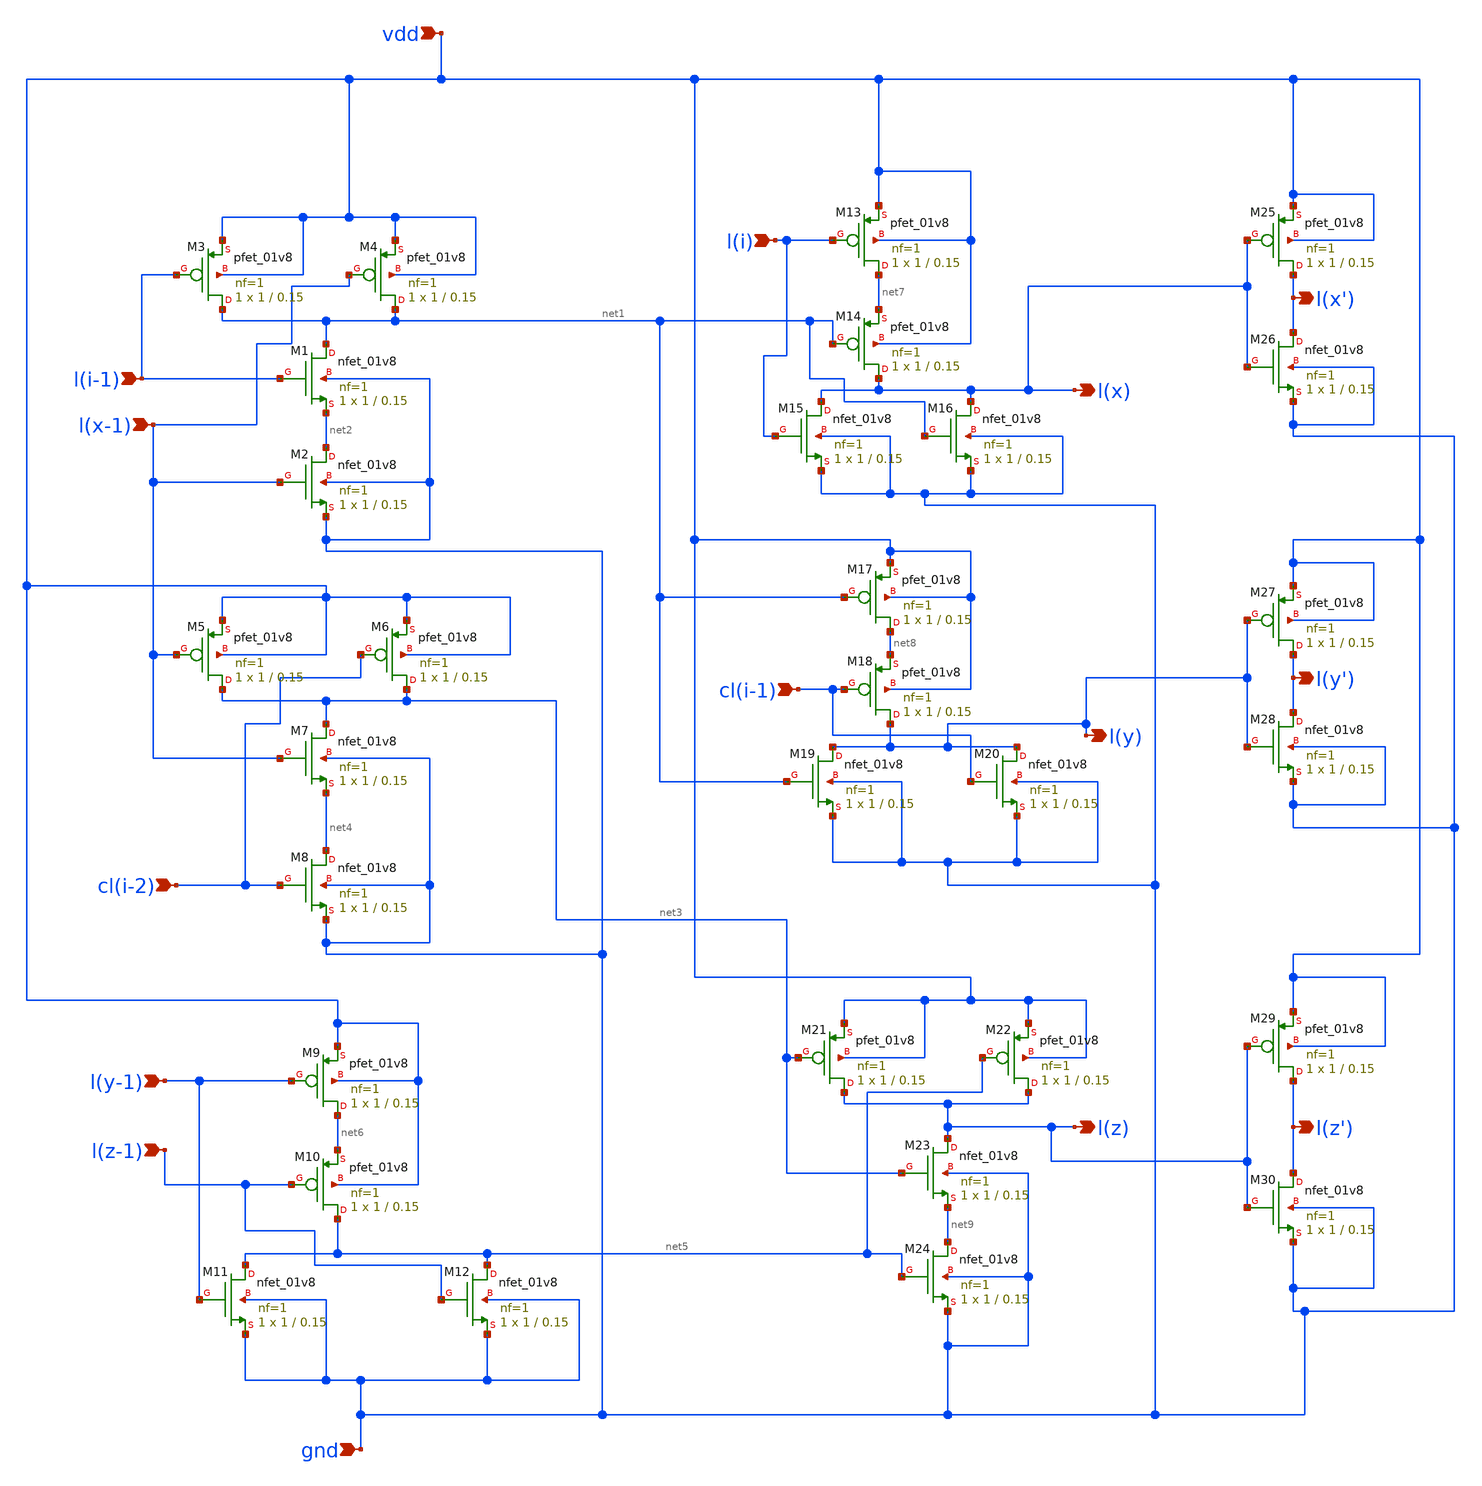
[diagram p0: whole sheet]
** sch_path: config_block2.sch
**.subckt config_block2 l(i-1) l(x-1) l(y-1) l(z-1) vdd gnd l(i) cl(i-1) l(x) l(y) l(z) l(x') l(y') l(z') cl(i-2)
*.ipin l(i-1)
*.ipin l(x-1)
*.ipin l(y-1)
*.ipin l(z-1)
*.ipin vdd
*.ipin gnd
*.ipin l(i)
*.ipin cl(i-1)
*.opin l(x)
*.opin l(y)
*.opin l(z)
*.opin l(x')
*.opin l(y')
*.opin l(z')
*.ipin cl(i-2)
XM1 net1 l(i-1) net2 gnd sky130_fd_pr__nfet_01v8 L=0.15 W=1 nf=1 ad='int((nf+1)/2) * W/nf * 0.29' as='int((nf+2)/2) * W/nf * 0.29'
+ pd='2*int((nf+1)/2) * (W/nf + 0.29)' ps='2*int((nf+2)/2) * (W/nf + 0.29)' nrd='0.29 / W' nrs='0.29 / W'
+ sa=0 sb=0 sd=0 mult=1 m=1
XM2 net2 l(x-1) gnd gnd sky130_fd_pr__nfet_01v8 L=0.15 W=1 nf=1 ad='int((nf+1)/2) * W/nf * 0.29' as='int((nf+2)/2) * W/nf * 0.29'
+ pd='2*int((nf+1)/2) * (W/nf + 0.29)' ps='2*int((nf+2)/2) * (W/nf + 0.29)' nrd='0.29 / W' nrs='0.29 / W'
+ sa=0 sb=0 sd=0 mult=1 m=1
XM3 net1 l(i-1) vdd vdd sky130_fd_pr__pfet_01v8 L=0.15 W=1 nf=1 ad='int((nf+1)/2) * W/nf * 0.29' as='int((nf+2)/2) * W/nf * 0.29'
+ pd='2*int((nf+1)/2) * (W/nf + 0.29)' ps='2*int((nf+2)/2) * (W/nf + 0.29)' nrd='0.29 / W' nrs='0.29 / W'
+ sa=0 sb=0 sd=0 mult=1 m=1
XM4 net1 l(x-1) vdd vdd sky130_fd_pr__pfet_01v8 L=0.15 W=1 nf=1 ad='int((nf+1)/2) * W/nf * 0.29' as='int((nf+2)/2) * W/nf * 0.29'
+ pd='2*int((nf+1)/2) * (W/nf + 0.29)' ps='2*int((nf+2)/2) * (W/nf + 0.29)' nrd='0.29 / W' nrs='0.29 / W'
+ sa=0 sb=0 sd=0 mult=1 m=1
XM5 net3 l(x-1) vdd vdd sky130_fd_pr__pfet_01v8 L=0.15 W=1 nf=1 ad='int((nf+1)/2) * W/nf * 0.29' as='int((nf+2)/2) * W/nf * 0.29'
+ pd='2*int((nf+1)/2) * (W/nf + 0.29)' ps='2*int((nf+2)/2) * (W/nf + 0.29)' nrd='0.29 / W' nrs='0.29 / W'
+ sa=0 sb=0 sd=0 mult=1 m=1
XM6 net3 cl(i-2) vdd vdd sky130_fd_pr__pfet_01v8 L=0.15 W=1 nf=1 ad='int((nf+1)/2) * W/nf * 0.29' as='int((nf+2)/2) * W/nf * 0.29'
+ pd='2*int((nf+1)/2) * (W/nf + 0.29)' ps='2*int((nf+2)/2) * (W/nf + 0.29)' nrd='0.29 / W' nrs='0.29 / W'
+ sa=0 sb=0 sd=0 mult=1 m=1
XM7 net3 l(x-1) net4 gnd sky130_fd_pr__nfet_01v8 L=0.15 W=1 nf=1 ad='int((nf+1)/2) * W/nf * 0.29' as='int((nf+2)/2) * W/nf * 0.29'
+ pd='2*int((nf+1)/2) * (W/nf + 0.29)' ps='2*int((nf+2)/2) * (W/nf + 0.29)' nrd='0.29 / W' nrs='0.29 / W'
+ sa=0 sb=0 sd=0 mult=1 m=1
XM8 net4 cl(i-2) gnd gnd sky130_fd_pr__nfet_01v8 L=0.15 W=1 nf=1 ad='int((nf+1)/2) * W/nf * 0.29' as='int((nf+2)/2) * W/nf * 0.29'
+ pd='2*int((nf+1)/2) * (W/nf + 0.29)' ps='2*int((nf+2)/2) * (W/nf + 0.29)' nrd='0.29 / W' nrs='0.29 / W'
+ sa=0 sb=0 sd=0 mult=1 m=1
XM9 net6 l(y-1) vdd vdd sky130_fd_pr__pfet_01v8 L=0.15 W=1 nf=1 ad='int((nf+1)/2) * W/nf * 0.29' as='int((nf+2)/2) * W/nf * 0.29'
+ pd='2*int((nf+1)/2) * (W/nf + 0.29)' ps='2*int((nf+2)/2) * (W/nf + 0.29)' nrd='0.29 / W' nrs='0.29 / W'
+ sa=0 sb=0 sd=0 mult=1 m=1
XM10 net5 l(z-1) net6 vdd sky130_fd_pr__pfet_01v8 L=0.15 W=1 nf=1 ad='int((nf+1)/2) * W/nf * 0.29' as='int((nf+2)/2) * W/nf * 0.29'
+ pd='2*int((nf+1)/2) * (W/nf + 0.29)' ps='2*int((nf+2)/2) * (W/nf + 0.29)' nrd='0.29 / W' nrs='0.29 / W'
+ sa=0 sb=0 sd=0 mult=1 m=1
XM11 net5 l(y-1) gnd gnd sky130_fd_pr__nfet_01v8 L=0.15 W=1 nf=1 ad='int((nf+1)/2) * W/nf * 0.29' as='int((nf+2)/2) * W/nf * 0.29'
+ pd='2*int((nf+1)/2) * (W/nf + 0.29)' ps='2*int((nf+2)/2) * (W/nf + 0.29)' nrd='0.29 / W' nrs='0.29 / W'
+ sa=0 sb=0 sd=0 mult=1 m=1
XM12 net5 l(z-1) gnd gnd sky130_fd_pr__nfet_01v8 L=0.15 W=1 nf=1 ad='int((nf+1)/2) * W/nf * 0.29' as='int((nf+2)/2) * W/nf * 0.29'
+ pd='2*int((nf+1)/2) * (W/nf + 0.29)' ps='2*int((nf+2)/2) * (W/nf + 0.29)' nrd='0.29 / W' nrs='0.29 / W'
+ sa=0 sb=0 sd=0 mult=1 m=1
XM13 net7 l(i) vdd vdd sky130_fd_pr__pfet_01v8 L=0.15 W=1 nf=1 ad='int((nf+1)/2) * W/nf * 0.29' as='int((nf+2)/2) * W/nf * 0.29'
+ pd='2*int((nf+1)/2) * (W/nf + 0.29)' ps='2*int((nf+2)/2) * (W/nf + 0.29)' nrd='0.29 / W' nrs='0.29 / W'
+ sa=0 sb=0 sd=0 mult=1 m=1
XM14 l(x) net1 net7 vdd sky130_fd_pr__pfet_01v8 L=0.15 W=1 nf=1 ad='int((nf+1)/2) * W/nf * 0.29' as='int((nf+2)/2) * W/nf * 0.29'
+ pd='2*int((nf+1)/2) * (W/nf + 0.29)' ps='2*int((nf+2)/2) * (W/nf + 0.29)' nrd='0.29 / W' nrs='0.29 / W'
+ sa=0 sb=0 sd=0 mult=1 m=1
XM15 l(x) l(i) gnd gnd sky130_fd_pr__nfet_01v8 L=0.15 W=1 nf=1 ad='int((nf+1)/2) * W/nf * 0.29' as='int((nf+2)/2) * W/nf * 0.29'
+ pd='2*int((nf+1)/2) * (W/nf + 0.29)' ps='2*int((nf+2)/2) * (W/nf + 0.29)' nrd='0.29 / W' nrs='0.29 / W'
+ sa=0 sb=0 sd=0 mult=1 m=1
XM16 l(x) net1 gnd gnd sky130_fd_pr__nfet_01v8 L=0.15 W=1 nf=1 ad='int((nf+1)/2) * W/nf * 0.29' as='int((nf+2)/2) * W/nf * 0.29'
+ pd='2*int((nf+1)/2) * (W/nf + 0.29)' ps='2*int((nf+2)/2) * (W/nf + 0.29)' nrd='0.29 / W' nrs='0.29 / W'
+ sa=0 sb=0 sd=0 mult=1 m=1
XM17 net8 net1 vdd vdd sky130_fd_pr__pfet_01v8 L=0.15 W=1 nf=1 ad='int((nf+1)/2) * W/nf * 0.29' as='int((nf+2)/2) * W/nf * 0.29'
+ pd='2*int((nf+1)/2) * (W/nf + 0.29)' ps='2*int((nf+2)/2) * (W/nf + 0.29)' nrd='0.29 / W' nrs='0.29 / W'
+ sa=0 sb=0 sd=0 mult=1 m=1
XM18 l(y) cl(i-1) net8 vdd sky130_fd_pr__pfet_01v8 L=0.15 W=1 nf=1 ad='int((nf+1)/2) * W/nf * 0.29' as='int((nf+2)/2) * W/nf * 0.29'
+ pd='2*int((nf+1)/2) * (W/nf + 0.29)' ps='2*int((nf+2)/2) * (W/nf + 0.29)' nrd='0.29 / W' nrs='0.29 / W'
+ sa=0 sb=0 sd=0 mult=1 m=1
XM19 l(y) net1 gnd gnd sky130_fd_pr__nfet_01v8 L=0.15 W=1 nf=1 ad='int((nf+1)/2) * W/nf * 0.29' as='int((nf+2)/2) * W/nf * 0.29'
+ pd='2*int((nf+1)/2) * (W/nf + 0.29)' ps='2*int((nf+2)/2) * (W/nf + 0.29)' nrd='0.29 / W' nrs='0.29 / W'
+ sa=0 sb=0 sd=0 mult=1 m=1
XM20 l(y) cl(i-1) gnd gnd sky130_fd_pr__nfet_01v8 L=0.15 W=1 nf=1 ad='int((nf+1)/2) * W/nf * 0.29' as='int((nf+2)/2) * W/nf * 0.29'
+ pd='2*int((nf+1)/2) * (W/nf + 0.29)' ps='2*int((nf+2)/2) * (W/nf + 0.29)' nrd='0.29 / W' nrs='0.29 / W'
+ sa=0 sb=0 sd=0 mult=1 m=1
XM21 l(z) net3 vdd vdd sky130_fd_pr__pfet_01v8 L=0.15 W=1 nf=1 ad='int((nf+1)/2) * W/nf * 0.29' as='int((nf+2)/2) * W/nf * 0.29'
+ pd='2*int((nf+1)/2) * (W/nf + 0.29)' ps='2*int((nf+2)/2) * (W/nf + 0.29)' nrd='0.29 / W' nrs='0.29 / W'
+ sa=0 sb=0 sd=0 mult=1 m=1
XM22 l(z) net5 vdd vdd sky130_fd_pr__pfet_01v8 L=0.15 W=1 nf=1 ad='int((nf+1)/2) * W/nf * 0.29' as='int((nf+2)/2) * W/nf * 0.29'
+ pd='2*int((nf+1)/2) * (W/nf + 0.29)' ps='2*int((nf+2)/2) * (W/nf + 0.29)' nrd='0.29 / W' nrs='0.29 / W'
+ sa=0 sb=0 sd=0 mult=1 m=1
XM23 l(z) net3 net9 gnd sky130_fd_pr__nfet_01v8 L=0.15 W=1 nf=1 ad='int((nf+1)/2) * W/nf * 0.29' as='int((nf+2)/2) * W/nf * 0.29'
+ pd='2*int((nf+1)/2) * (W/nf + 0.29)' ps='2*int((nf+2)/2) * (W/nf + 0.29)' nrd='0.29 / W' nrs='0.29 / W'
+ sa=0 sb=0 sd=0 mult=1 m=1
XM24 net9 net5 gnd gnd sky130_fd_pr__nfet_01v8 L=0.15 W=1 nf=1 ad='int((nf+1)/2) * W/nf * 0.29' as='int((nf+2)/2) * W/nf * 0.29'
+ pd='2*int((nf+1)/2) * (W/nf + 0.29)' ps='2*int((nf+2)/2) * (W/nf + 0.29)' nrd='0.29 / W' nrs='0.29 / W'
+ sa=0 sb=0 sd=0 mult=1 m=1
XM25 l(x') l(x) vdd vdd sky130_fd_pr__pfet_01v8 L=0.15 W=1 nf=1 ad='int((nf+1)/2) * W/nf * 0.29' as='int((nf+2)/2)
+ * W/nf * 0.29' pd='2*int((nf+1)/2) * (W/nf + 0.29)' ps='2*int((nf+2)/2) * (W/nf + 0.29)' nrd='0.29 /
+ W' nrs='0.29 / W' sa=0 sb=0 sd=0 mult=1 m=1
XM26 l(x') l(x) gnd gnd sky130_fd_pr__nfet_01v8 L=0.15 W=1 nf=1 ad='int((nf+1)/2) * W/nf * 0.29' as='int((nf+2)/2) * W/nf * 0.29'
+ pd='2*int((nf+1)/2) * (W/nf + 0.29)' ps='2*int((nf+2)/2) * (W/nf + 0.29)' nrd='0.29 / W' nrs='0.29 / W'
+ sa=0 sb=0 sd=0 mult=1 m=1
XM27 l(y') l(y) vdd vdd sky130_fd_pr__pfet_01v8 L=0.15 W=1 nf=1 ad='int((nf+1)/2) * W/nf * 0.29' as='int((nf+2)/2)
+ * W/nf * 0.29' pd='2*int((nf+1)/2) * (W/nf + 0.29)' ps='2*int((nf+2)/2) * (W/nf + 0.29)' nrd='0.29 /
+ W' nrs='0.29 / W' sa=0 sb=0 sd=0 mult=1 m=1
XM28 l(y') l(y) gnd gnd sky130_fd_pr__nfet_01v8 L=0.15 W=1 nf=1 ad='int((nf+1)/2) * W/nf * 0.29' as='int((nf+2)/2) * W/nf * 0.29'
+ pd='2*int((nf+1)/2) * (W/nf + 0.29)' ps='2*int((nf+2)/2) * (W/nf + 0.29)' nrd='0.29 / W' nrs='0.29 / W'
+ sa=0 sb=0 sd=0 mult=1 m=1
XM29 l(z') l(z) vdd vdd sky130_fd_pr__pfet_01v8 L=0.15 W=1 nf=1 ad='int((nf+1)/2) * W/nf * 0.29' as='int((nf+2)/2)
+ * W/nf * 0.29' pd='2*int((nf+1)/2) * (W/nf + 0.29)' ps='2*int((nf+2)/2) * (W/nf + 0.29)' nrd='0.29 /
+ W' nrs='0.29 / W' sa=0 sb=0 sd=0 mult=1 m=1
XM30 l(z') l(z) gnd gnd sky130_fd_pr__nfet_01v8 L=0.15 W=1 nf=1 ad='int((nf+1)/2) * W/nf * 0.29' as='int((nf+2)/2) * W/nf * 0.29'
+ pd='2*int((nf+1)/2) * (W/nf + 0.29)' ps='2*int((nf+2)/2) * (W/nf + 0.29)' nrd='0.29 / W' nrs='0.29 / W'
+ sa=0 sb=0 sd=0 mult=1 m=1
**.ends
.end
